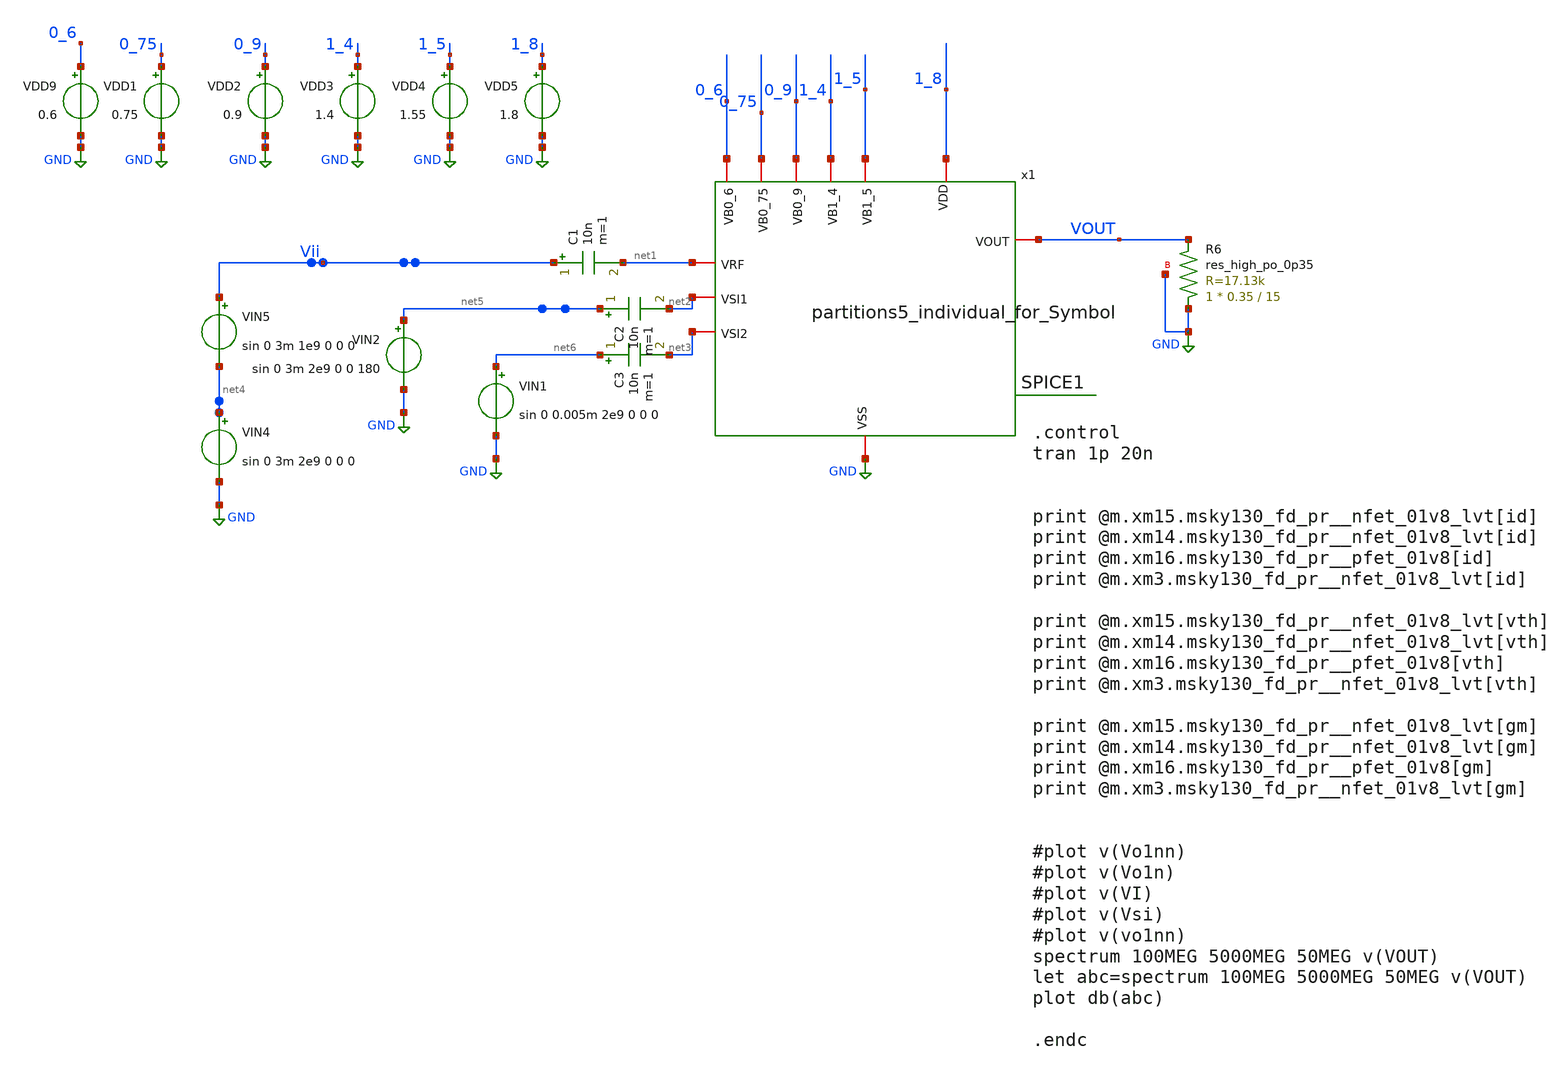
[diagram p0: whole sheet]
** sch_path: xschem/xschem4_sic_oct_20/TB_tran.sch
**.subckt TB_tran
x1 1_8 0_6 VOUT net3 1_5 0_9 1_4 net1 net2 0_75 GND partitions5_individual_for_Symbol
VDD9 0_6 GND 0.6
VDD1 0_75 GND 0.75
VDD2 0_9 GND 0.9
VDD3 1_4 GND 1.4
VDD4 1_5 GND 1.55
VDD5 1_8 GND 1.8
C1 Vii net1 10n m=1
VIN4 net4 GND sin 0 3m 2e9 0 0 0
VIN5 Vii net4 sin 0 3m 1e9 0 0 0
VIN2 net5 GND sin 0 3m 2e9 0 0 180
C2 net5 net2 10n m=1
VIN1 net6 GND sin 0 0.005m 2e9 0 0 0
C3 net6 net3 10n m=1
XR6 GND VOUT GND sky130_fd_pr__res_high_po_0p35 L=15 mult=1 m=1
**** begin user architecture code

.lib $::SKYWATER_MODELS/sky130.lib.spice ff



.control
tran 1p 20n


print @m.xm15.msky130_fd_pr__nfet_01v8_lvt[id]
print @m.xm14.msky130_fd_pr__nfet_01v8_lvt[id]
print @m.xm16.msky130_fd_pr__pfet_01v8[id]
print @m.xm3.msky130_fd_pr__nfet_01v8_lvt[id]

print @m.xm15.msky130_fd_pr__nfet_01v8_lvt[vth]
print @m.xm14.msky130_fd_pr__nfet_01v8_lvt[vth]
print @m.xm16.msky130_fd_pr__pfet_01v8[vth]
print @m.xm3.msky130_fd_pr__nfet_01v8_lvt[vth]

print @m.xm15.msky130_fd_pr__nfet_01v8_lvt[gm]
print @m.xm14.msky130_fd_pr__nfet_01v8_lvt[gm]
print @m.xm16.msky130_fd_pr__pfet_01v8[gm]
print @m.xm3.msky130_fd_pr__nfet_01v8_lvt[gm]


#plot v(Vo1nn)
#plot v(Vo1n)
#plot v(VI)
#plot v(Vsi)
#plot v(vo1nn)
spectrum 100MEG 5000MEG 50MEG v(VOUT)
let abc=spectrum 100MEG 5000MEG 50MEG v(VOUT)
plot db(abc)

.endc


**** end user architecture code
**.ends

* expanding   symbol:  partitions5_individual_for_Symbol.sym # of pins=11
** sym_path: xschem/xschem4_sic_oct_20/partitions5_individual_for_Symbol.sym
** sch_path: xschem/xschem4_sic_oct_20/partitions5_individual_for_Symbol.sch
.subckt partitions5_individual_for_Symbol VDD VB0_6 VOUT VSI2 VB1_5 VB0_9 VB1_4 VRF VSI1 VB0_75 VSS
*.iopin VRF
*.iopin VSS
*.iopin VB0_75
*.iopin VSI1
*.iopin VB1_4
*.iopin VDD
*.iopin VB1_5
*.iopin VB0_9
*.iopin VSI2
*.iopin VB0_6
*.iopin VOUT
XM12 net1 VRF VSS VSS sky130_fd_pr__nfet_01v8_lvt L=0.15 W=220 nf=22 ad='int((nf+1)/2) * W/nf * 0.29'
+ as='int((nf+2)/2) * W/nf * 0.29' pd='2*int((nf+1)/2) * (W/nf + 0.29)' ps='2*int((nf+2)/2) * (W/nf + 0.29)'
+ nrd='0.29 / W' nrs='0.29 / W' sa=0 sb=0 sd=0 mult=1 m=1
XM13 net1 VRF VDD VDD sky130_fd_pr__pfet_01v8 L=0.15 W=30 nf=3 ad='int((nf+1)/2) * W/nf * 0.29' as='int((nf+2)/2) * W/nf * 0.29'
+ pd='2*int((nf+1)/2) * (W/nf + 0.29)' ps='2*int((nf+2)/2) * (W/nf + 0.29)' nrd='0.29 / W' nrs='0.29 / W'
+ sa=0 sb=0 sd=0 mult=1 m=1
XM14 VOUT1 VB1_4 net1 VSS sky130_fd_pr__nfet_01v8_lvt L=0.15 W=80 nf=8 ad='int((nf+1)/2) * W/nf * 0.29'
+ as='int((nf+2)/2) * W/nf * 0.29' pd='2*int((nf+1)/2) * (W/nf + 0.29)' ps='2*int((nf+2)/2) * (W/nf + 0.29)'
+ nrd='0.29 / W' nrs='0.29 / W' sa=0 sb=0 sd=0 mult=1 m=1
XM16 VRF VB0_75 VSS VSS sky130_fd_pr__nfet_01v8_lvt L=0.15 W=7.8 nf=1 ad='int((nf+1)/2) * W/nf * 0.29'
+ as='int((nf+2)/2) * W/nf * 0.29' pd='2*int((nf+1)/2) * (W/nf + 0.29)' ps='2*int((nf+2)/2) * (W/nf + 0.29)'
+ nrd='0.29 / W' nrs='0.29 / W' sa=0 sb=0 sd=0 mult=1 m=1
XM20 net1 VSI1 VSS VSS sky130_fd_pr__nfet_01v8_lvt L=0.15 W=240 nf=24 ad='int((nf+1)/2) * W/nf * 0.29'
+ as='int((nf+2)/2) * W/nf * 0.29' pd='2*int((nf+1)/2) * (W/nf + 0.29)' ps='2*int((nf+2)/2) * (W/nf + 0.29)'
+ nrd='0.29 / W' nrs='0.29 / W' sa=0 sb=0 sd=0 mult=1 m=1
XR16 VB0_75 VSI1 VSS sky130_fd_pr__res_high_po_0p35 L=6.2 mult=1 m=1
XR4 VB1_5 net2 VSS sky130_fd_pr__res_high_po_0p35 L=4 mult=1 m=1
XC5 net2 VOUT1 sky130_fd_pr__cap_mim_m3_2 W=30 L=30 MF=1 m=1
XM15 net3 net2 VRF VSS sky130_fd_pr__nfet_01v8_lvt L=0.15 W=7.8 nf=1 ad='int((nf+1)/2) * W/nf * 0.29'
+ as='int((nf+2)/2) * W/nf * 0.29' pd='2*int((nf+1)/2) * (W/nf + 0.29)' ps='2*int((nf+2)/2) * (W/nf + 0.29)'
+ nrd='0.29 / W' nrs='0.29 / W' sa=0 sb=0 sd=0 mult=1 m=1
XR14 net3 VDD VSS sky130_fd_pr__res_high_po_0p35 L=0.5 mult=1 m=1
XR15 VOUT1 VDD VSS sky130_fd_pr__res_high_po_0p69 L=0.69 mult=8 m=8
XM21 VOUT2 VOUT1 VSS VSS sky130_fd_pr__nfet_01v8_lvt L=0.15 W=7.8 nf=1 ad='int((nf+1)/2) * W/nf * 0.29'
+ as='int((nf+2)/2) * W/nf * 0.29' pd='2*int((nf+1)/2) * (W/nf + 0.29)' ps='2*int((nf+2)/2) * (W/nf + 0.29)'
+ nrd='0.29 / W' nrs='0.29 / W' sa=0 sb=0 sd=0 mult=1 m=1
XR17 VOUT2 VDD VSS sky130_fd_pr__res_high_po_0p35 L=0.5 mult=1 m=1
XM17 net5 net6 VSS VSS sky130_fd_pr__nfet_01v8_lvt L=0.15 W=45 nf=7 ad='int((nf+1)/2) * W/nf * 0.29'
+ as='int((nf+2)/2) * W/nf * 0.29' pd='2*int((nf+1)/2) * (W/nf + 0.29)' ps='2*int((nf+2)/2) * (W/nf + 0.29)'
+ nrd='0.29 / W' nrs='0.29 / W' sa=0 sb=0 sd=0 mult=1 m=1
XM18 VDD net4 net5 VSS sky130_fd_pr__nfet_01v8_lvt L=0.15 W=12 nf=3 ad='int((nf+1)/2) * W/nf * 0.29'
+ as='int((nf+2)/2) * W/nf * 0.29' pd='2*int((nf+1)/2) * (W/nf + 0.29)' ps='2*int((nf+2)/2) * (W/nf + 0.29)'
+ nrd='0.29 / W' nrs='0.29 / W' sa=0 sb=0 sd=0 mult=1 m=1
XR11 net4 VDD VSS sky130_fd_pr__res_high_po_0p35 L=15 mult=1 m=1
XC7 VOUT2 net4 sky130_fd_pr__cap_mim_m3_2 W=30 L=30 MF=1 m=1
XR12 VB0_9 net6 VSS sky130_fd_pr__res_high_po_0p35 L=8 mult=1 m=1
XC8 VOUT1 net6 sky130_fd_pr__cap_mim_m3_2 W=30 L=30 MF=1 m=1
XD1 VSS net4 sky130_fd_pr__diode_pw2nd_05v5 area=1e12 pj=4e6
XM19 net5 net7 VDD VDD sky130_fd_pr__pfet_01v8 L=0.15 W=30 nf=3 ad='int((nf+1)/2) * W/nf * 0.29' as='int((nf+2)/2) * W/nf * 0.29'
+ pd='2*int((nf+1)/2) * (W/nf + 0.29)' ps='2*int((nf+2)/2) * (W/nf + 0.29)' nrd='0.29 / W' nrs='0.29 / W'
+ sa=0 sb=0 sd=0 mult=1 m=1
XR13 VB0_6 net7 VSS sky130_fd_pr__res_high_po_0p35 L=6.2 mult=1 m=1
XM22 net5 VSI2 VSS VSS sky130_fd_pr__nfet_01v8_lvt L=0.15 W=80 nf=8 ad='int((nf+1)/2) * W/nf * 0.29'
+ as='int((nf+2)/2) * W/nf * 0.29' pd='2*int((nf+1)/2) * (W/nf + 0.29)' ps='2*int((nf+2)/2) * (W/nf + 0.29)'
+ nrd='0.29 / W' nrs='0.29 / W' sa=0 sb=0 sd=0 mult=1 m=1
XR18 VB0_75 VSI2 VSS sky130_fd_pr__res_high_po_0p35 L=0.5 mult=1 m=1
XM4 VDD net8 VOUT VSS sky130_fd_pr__nfet_01v8_lvt L=0.15 W=100 nf=10 ad='int((nf+1)/2) * W/nf * 0.29'
+ as='int((nf+2)/2) * W/nf * 0.29' pd='2*int((nf+1)/2) * (W/nf + 0.29)' ps='2*int((nf+2)/2) * (W/nf + 0.29)'
+ nrd='0.29 / W' nrs='0.29 / W' sa=0 sb=0 sd=0 mult=1 m=1
XR5 net8 VDD VSS sky130_fd_pr__res_high_po_0p35 L=4 mult=1 m=1
XR6 VSS VOUT VSS sky130_fd_pr__res_high_po_0p35 L=15 mult=1 m=1
XC3 net5 net8 sky130_fd_pr__cap_mim_m3_2 W=30 L=30 MF=1 m=1
.ends

.GLOBAL GND
.end
